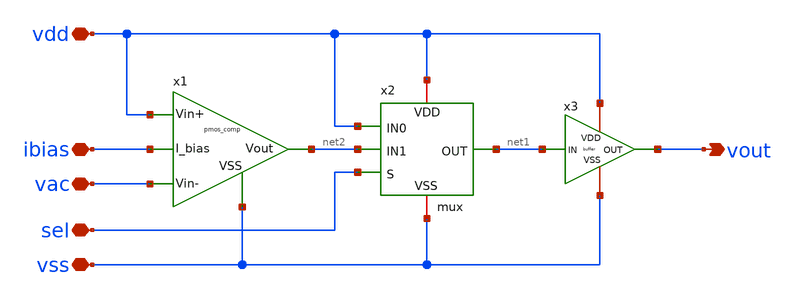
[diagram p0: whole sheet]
** sch_path: Layouts/driver/driver.sch
**.subckt driver vdd ibias vac sel vss vout
*.iopin vdd
*.iopin ibias
*.iopin vac
*.iopin sel
*.iopin vss
*.opin vout
x1 vac vdd net2 ibias vss pmos_comp
x2 vdd vdd sel net1 net2 vss mux
x3 vdd net1 vout vss buffer wn=1u
**.ends
.end
